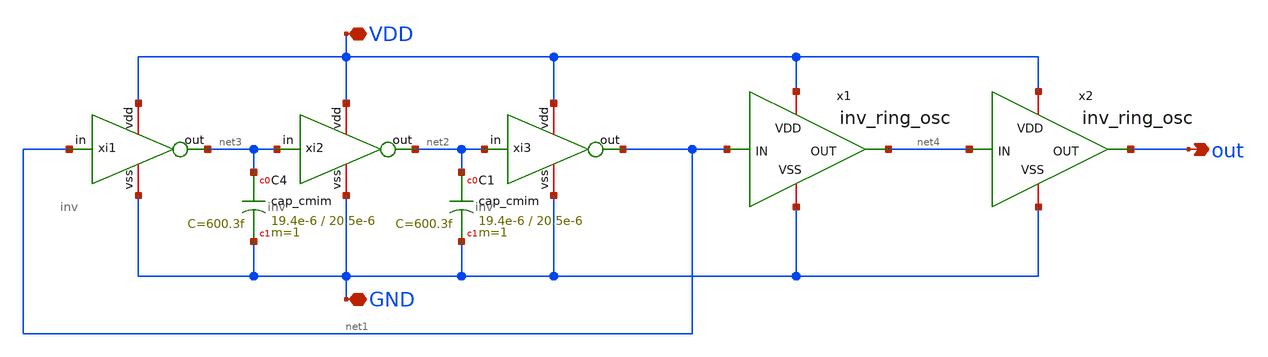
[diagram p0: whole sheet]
** sch_path: SSDOR_1.2V_v2/components/cgenerator/clk_ringosc.sch
**.subckt clk_ringosc GND VDD out
*.iopin GND
*.iopin VDD
*.opin out
xi1 VDD net1 net3 GND inv
xi2 VDD net3 net2 GND inv
xi3 VDD net2 net1 GND inv
x1 VDD net1 net4 GND inv_ring_osc
x2 VDD net4 out GND inv_ring_osc
XC4 net3 GND cap_cmim w=19.4e-6 l=20.5e-6 m=1 mm_ok=1
XC1 net2 GND cap_cmim w=19.4e-6 l=20.5e-6 m=1 mm_ok=1
**.ends
.end
